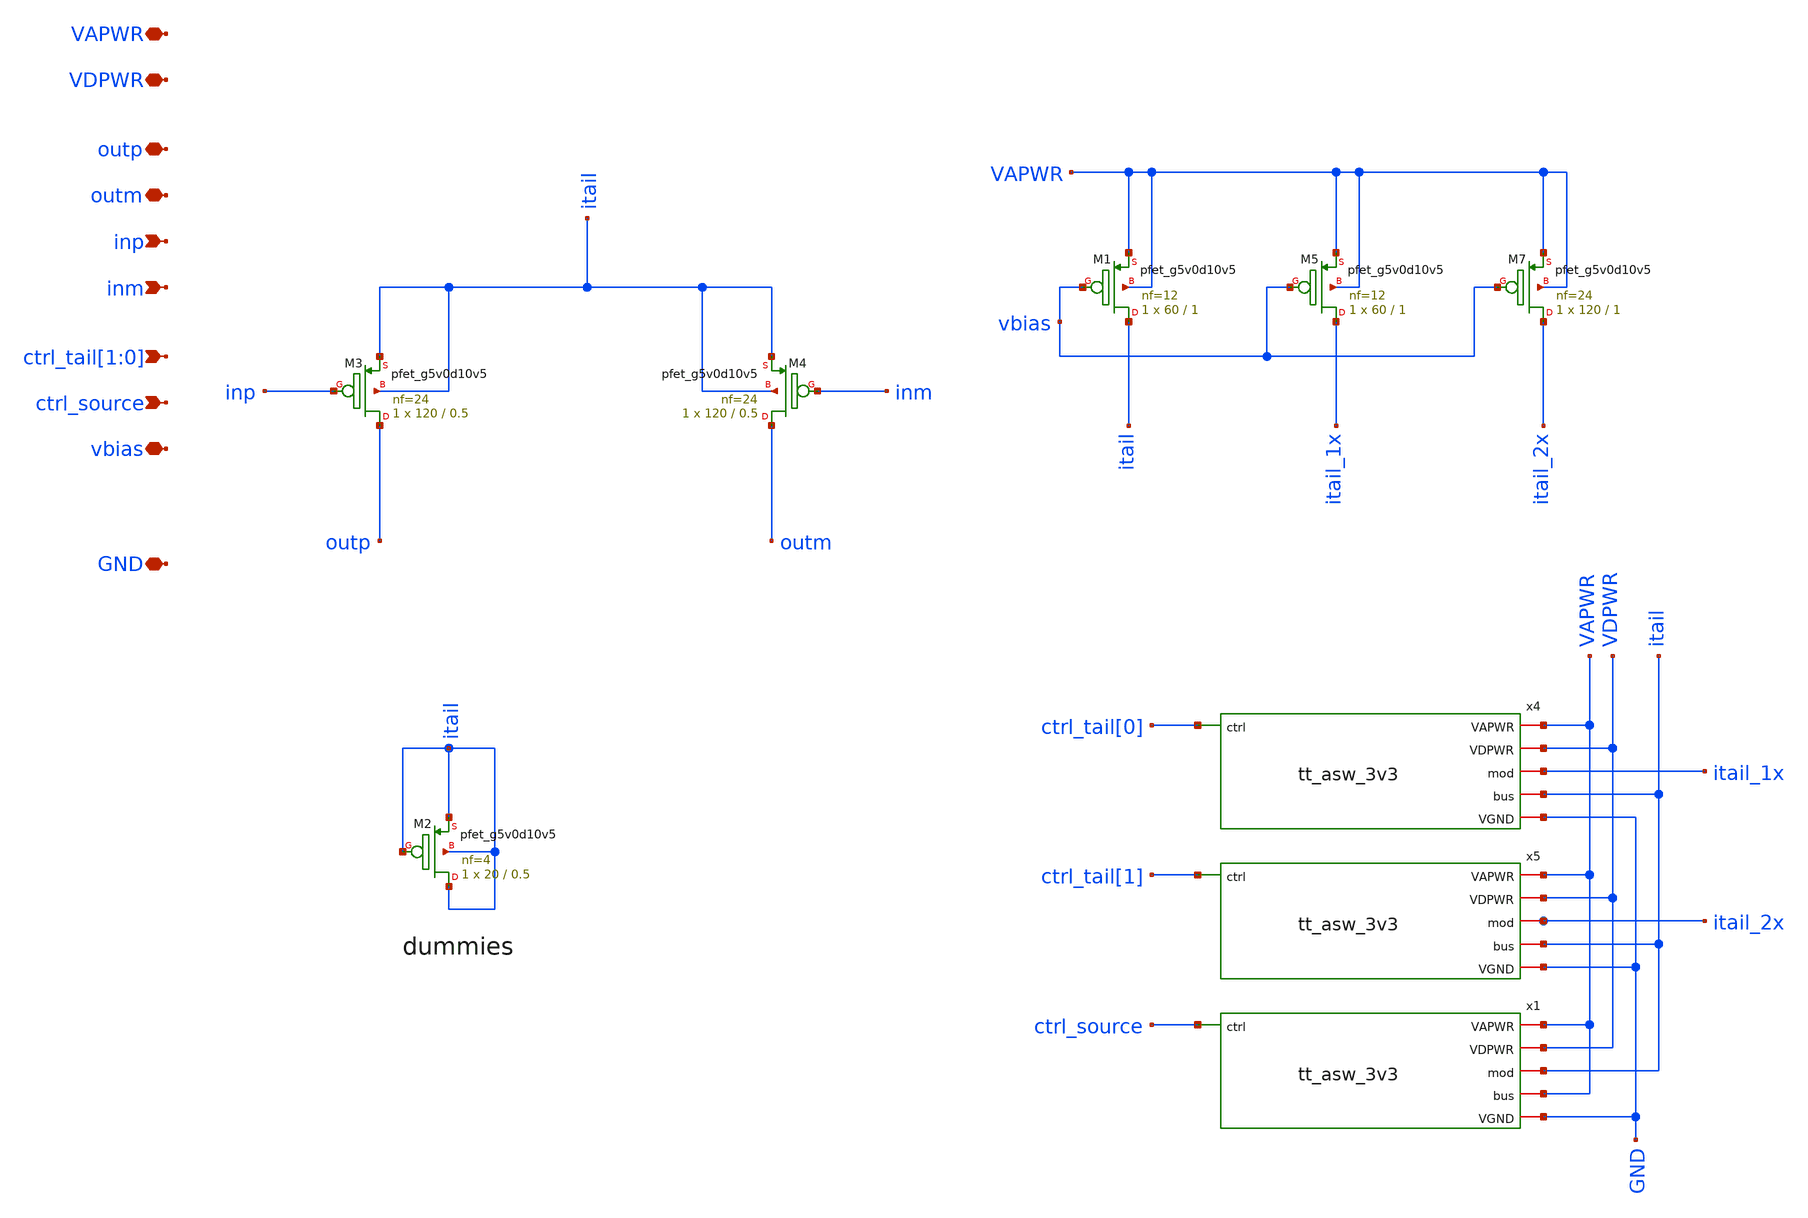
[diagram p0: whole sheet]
** sch_path: tt_um_mosbius/xschem/diff_p.sch
**.subckt diff_p vbias ctrl_tail[1],ctrl_tail[0] VAPWR VDPWR GND ctrl_source inp inm outp outm
*.iopin vbias
*.ipin ctrl_tail[1],ctrl_tail[0]
*.iopin VAPWR
*.iopin VDPWR
*.iopin GND
*.ipin ctrl_source
*.ipin inp
*.ipin inm
*.iopin outp
*.iopin outm
x4 GND VDPWR VAPWR ctrl_tail[0] itail_1x itail tt_asw_3v3
x5 GND VDPWR VAPWR ctrl_tail[1] itail_2x itail tt_asw_3v3
x1 GND VDPWR VAPWR ctrl_source itail VAPWR tt_asw_3v3
XM3 outp inp itail itail sky130_fd_pr__pfet_g5v0d10v5 L=0.5 W=120 nf=24 ad='int((nf+1)/2) * W/nf * 0.29'
+ as='int((nf+2)/2) * W/nf * 0.29' pd='2*int((nf+1)/2) * (W/nf + 0.29)' ps='2*int((nf+2)/2) * (W/nf + 0.29)'
+ nrd='0.29 / W' nrs='0.29 / W' sa=0 sb=0 sd=0 mult=1 m=1
XM4 outm inm itail itail sky130_fd_pr__pfet_g5v0d10v5 L=0.5 W=120 nf=24 ad='int((nf+1)/2) * W/nf * 0.29'
+ as='int((nf+2)/2) * W/nf * 0.29' pd='2*int((nf+1)/2) * (W/nf + 0.29)' ps='2*int((nf+2)/2) * (W/nf + 0.29)'
+ nrd='0.29 / W' nrs='0.29 / W' sa=0 sb=0 sd=0 mult=1 m=1
XM1 itail vbias VAPWR VAPWR sky130_fd_pr__pfet_g5v0d10v5 L=1 W=60 nf=12 ad='int((nf+1)/2) * W/nf * 0.29'
+ as='int((nf+2)/2) * W/nf * 0.29' pd='2*int((nf+1)/2) * (W/nf + 0.29)' ps='2*int((nf+2)/2) * (W/nf + 0.29)'
+ nrd='0.29 / W' nrs='0.29 / W' sa=0 sb=0 sd=0 mult=1 m=1
XM5 itail_1x vbias VAPWR VAPWR sky130_fd_pr__pfet_g5v0d10v5 L=1 W=60 nf=12 ad='int((nf+1)/2) * W/nf * 0.29'
+ as='int((nf+2)/2) * W/nf * 0.29' pd='2*int((nf+1)/2) * (W/nf + 0.29)' ps='2*int((nf+2)/2) * (W/nf + 0.29)'
+ nrd='0.29 / W' nrs='0.29 / W' sa=0 sb=0 sd=0 mult=1 m=1
XM7 itail_2x vbias VAPWR VAPWR sky130_fd_pr__pfet_g5v0d10v5 L=1 W=120 nf=24 ad='int((nf+1)/2) * W/nf * 0.29'
+ as='int((nf+2)/2) * W/nf * 0.29' pd='2*int((nf+1)/2) * (W/nf + 0.29)' ps='2*int((nf+2)/2) * (W/nf + 0.29)'
+ nrd='0.29 / W' nrs='0.29 / W' sa=0 sb=0 sd=0 mult=1 m=1
XM2 itail itail itail itail sky130_fd_pr__pfet_g5v0d10v5 L=0.5 W=20 nf=4 ad='int((nf+1)/2) * W/nf * 0.29'
+ as='int((nf+2)/2) * W/nf * 0.29' pd='2*int((nf+1)/2) * (W/nf + 0.29)' ps='2*int((nf+2)/2) * (W/nf + 0.29)'
+ nrd='0.29 / W' nrs='0.29 / W' sa=0 sb=0 sd=0 mult=1 m=1
**.ends

* expanding   symbol:  tt_asw_3v3.sym # of pins=6
** sym_path: tt_asw_3v3.sym
** sch_path: tt_asw_3v3.sch
.subckt tt_asw_3v3 VGND VDPWR VAPWR ctrl mod bus
*.iopin mod
*.iopin bus
*.ipin ctrl
*.iopin VGND
*.iopin VDPWR
*.iopin VAPWR
XM1 tgon_n net2 VAPWR VAPWR sky130_fd_pr__pfet_g5v0d10v5 L=0.5 W=0.84 nf=1 ad='int((nf+1)/2) * W/nf * 0.29'
+ as='int((nf+2)/2) * W/nf * 0.29' pd='2*int((nf+1)/2) * (W/nf + 0.29)' ps='2*int((nf+2)/2) * (W/nf + 0.29)'
+ nrd='0.29 / W' nrs='0.29 / W' sa=0 sb=0 sd=0 mult=1 m=1
XM2 tgon_n net2 VGND VGND sky130_fd_pr__nfet_g5v0d10v5 L=0.5 W=0.42 nf=1 ad='int((nf+1)/2) * W/nf * 0.29'
+ as='int((nf+2)/2) * W/nf * 0.29' pd='2*int((nf+1)/2) * (W/nf + 0.29)' ps='2*int((nf+2)/2) * (W/nf + 0.29)'
+ nrd='0.29 / W' nrs='0.29 / W' sa=0 sb=0 sd=0 mult=1 m=1
XM3 tgon net1 VAPWR VAPWR sky130_fd_pr__pfet_g5v0d10v5 L=0.5 W=0.84 nf=1 ad='int((nf+1)/2) * W/nf * 0.29'
+ as='int((nf+2)/2) * W/nf * 0.29' pd='2*int((nf+1)/2) * (W/nf + 0.29)' ps='2*int((nf+2)/2) * (W/nf + 0.29)'
+ nrd='0.29 / W' nrs='0.29 / W' sa=0 sb=0 sd=0 mult=1 m=1
XM4 tgon net1 VGND VGND sky130_fd_pr__nfet_g5v0d10v5 L=0.5 W=0.42 nf=1 ad='int((nf+1)/2) * W/nf * 0.29'
+ as='int((nf+2)/2) * W/nf * 0.29' pd='2*int((nf+1)/2) * (W/nf + 0.29)' ps='2*int((nf+2)/2) * (W/nf + 0.29)'
+ nrd='0.29 / W' nrs='0.29 / W' sa=0 sb=0 sd=0 mult=1 m=1
XM5 bus tgon_n mod VAPWR sky130_fd_pr__pfet_g5v0d10v5 L=0.5 W=180 nf=18 ad='int((nf+1)/2) * W/nf * 0.29'
+ as='int((nf+2)/2) * W/nf * 0.29' pd='2*int((nf+1)/2) * (W/nf + 0.29)' ps='2*int((nf+2)/2) * (W/nf + 0.29)'
+ nrd='0.29 / W' nrs='0.29 / W' sa=0 sb=0 sd=0 mult=1 m=1
XM6 bus tgon mod VGND sky130_fd_pr__nfet_g5v0d10v5 L=0.5 W=60 nf=12 ad='int((nf+1)/2) * W/nf * 0.29'
+ as='int((nf+2)/2) * W/nf * 0.29' pd='2*int((nf+1)/2) * (W/nf + 0.29)' ps='2*int((nf+2)/2) * (W/nf + 0.29)'
+ nrd='0.29 / W' nrs='0.29 / W' sa=0 sb=0 sd=0 mult=1 m=1
XM7 ctrl_n ctrl VGND VGND sky130_fd_pr__nfet_01v8 L=0.15 W=0.42 nf=1 ad='int((nf+1)/2) * W/nf * 0.29'
+ as='int((nf+2)/2) * W/nf * 0.29' pd='2*int((nf+1)/2) * (W/nf + 0.29)' ps='2*int((nf+2)/2) * (W/nf + 0.29)'
+ nrd='0.29 / W' nrs='0.29 / W' sa=0 sb=0 sd=0 mult=1 m=1
XM8 ctrl_n ctrl VDPWR VDPWR sky130_fd_pr__pfet_01v8_hvt L=0.15 W=1 nf=1 ad='int((nf+1)/2) * W/nf * 0.29'
+ as='int((nf+2)/2) * W/nf * 0.29' pd='2*int((nf+1)/2) * (W/nf + 0.29)' ps='2*int((nf+2)/2) * (W/nf + 0.29)'
+ nrd='0.29 / W' nrs='0.29 / W' sa=0 sb=0 sd=0 mult=1 m=1
XM9 net1 ctrl VGND VGND sky130_fd_pr__nfet_g5v0d10v5 L=0.5 W=0.42 nf=1 ad='int((nf+1)/2) * W/nf * 0.29'
+ as='int((nf+2)/2) * W/nf * 0.29' pd='2*int((nf+1)/2) * (W/nf + 0.29)' ps='2*int((nf+2)/2) * (W/nf + 0.29)'
+ nrd='0.29 / W' nrs='0.29 / W' sa=0 sb=0 sd=0 mult=1 m=1
XM10 net2 ctrl_n VGND VGND sky130_fd_pr__nfet_g5v0d10v5 L=0.5 W=0.42 nf=1 ad='int((nf+1)/2) * W/nf * 0.29'
+ as='int((nf+2)/2) * W/nf * 0.29' pd='2*int((nf+1)/2) * (W/nf + 0.29)' ps='2*int((nf+2)/2) * (W/nf + 0.29)'
+ nrd='0.29 / W' nrs='0.29 / W' sa=0 sb=0 sd=0 mult=1 m=1
XM11 net1 net2 net3 VAPWR sky130_fd_pr__pfet_g5v0d10v5 L=0.5 W=0.42 nf=1 ad='int((nf+1)/2) * W/nf * 0.29'
+ as='int((nf+2)/2) * W/nf * 0.29' pd='2*int((nf+1)/2) * (W/nf + 0.29)' ps='2*int((nf+2)/2) * (W/nf + 0.29)'
+ nrd='0.29 / W' nrs='0.29 / W' sa=0 sb=0 sd=0 mult=1 m=1
XM12 net2 net1 net4 VAPWR sky130_fd_pr__pfet_g5v0d10v5 L=0.5 W=0.42 nf=1 ad='int((nf+1)/2) * W/nf * 0.29'
+ as='int((nf+2)/2) * W/nf * 0.29' pd='2*int((nf+1)/2) * (W/nf + 0.29)' ps='2*int((nf+2)/2) * (W/nf + 0.29)'
+ nrd='0.29 / W' nrs='0.29 / W' sa=0 sb=0 sd=0 mult=1 m=1
XM13 net3 net1 VAPWR VAPWR sky130_fd_pr__pfet_g5v0d10v5 L=0.5 W=0.42 nf=1 ad='int((nf+1)/2) * W/nf * 0.29'
+ as='int((nf+2)/2) * W/nf * 0.29' pd='2*int((nf+1)/2) * (W/nf + 0.29)' ps='2*int((nf+2)/2) * (W/nf + 0.29)'
+ nrd='0.29 / W' nrs='0.29 / W' sa=0 sb=0 sd=0 mult=1 m=1
XM14 net4 net2 VAPWR VAPWR sky130_fd_pr__pfet_g5v0d10v5 L=0.5 W=0.42 nf=1 ad='int((nf+1)/2) * W/nf * 0.29'
+ as='int((nf+2)/2) * W/nf * 0.29' pd='2*int((nf+1)/2) * (W/nf + 0.29)' ps='2*int((nf+2)/2) * (W/nf + 0.29)'
+ nrd='0.29 / W' nrs='0.29 / W' sa=0 sb=0 sd=0 mult=1 m=1
.ends

.end
